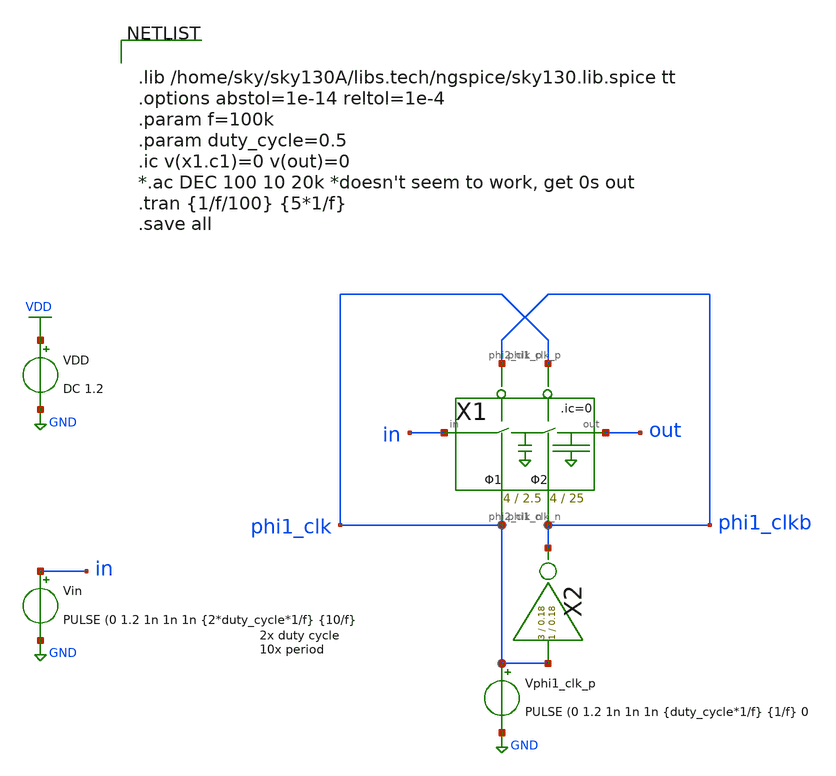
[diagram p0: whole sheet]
** sch_path: xschem/Switched_Caps/2switchcaps_tb.sch
**.subckt 2switchcaps_tb
Vin in GND PULSE (0 1.2 1n 1n 1n {2*duty_cycle*1/f} {10/f}
X1 in out phi1_clkb phi1_clk phi1_clkb phi1_clk 2switchcaps Wcap1=4 Lcap1=2.5 Wcap2=4 Lcap2=25
VDD VDD GND DC 1.2
X2 phi1_clk phi1_clkb inv Wpmos=3 Lpmos=0.18 Wnmos=1 Lnmos=0.18
Vphi1_clk_p phi1_clk GND PULSE (0 1.2 1n 1n 1n {duty_cycle*1/f} {1/f} 0
**** begin user architecture code


.lib /home/sky/sky130A/libs.tech/ngspice/sky130.lib.spice tt
.options abstol=1e-14 reltol=1e-4
.param f=100k
.param duty_cycle=0.5
.ic v(x1.c1)=0 v(out)=0
*.ac DEC 100 10 20k *doesn't seem to work, get 0s out
.tran {1/f/100} {5*1/f}
.save all


**** end user architecture code
**.ends

* expanding   symbol:  Switched_Caps/2switchcaps.sym # of pins=6
** sym_path: xschem/Switched_Caps/2switchcaps.sym
** sch_path: xschem/Switched_Caps/2switchcaps.sch
.subckt 2switchcaps in out phi2_clk_n phi1_clk_n phi1_clk_p phi2_clk_p  Wcap1=4 Lcap1=2.5 Wcap2=4 Lcap2=25
*.iopin out
*.iopin in
*.ipin phi1_clk_n
*.ipin phi1_clk_p
*.ipin phi2_clk_p
*.ipin phi2_clk_n
XC1 c1 GND sky130_fd_pr__cap_mim_m3_1 W=Wcap L=Lcap MF=1 m=1
XC2 out GND sky130_fd_pr__cap_mim_m3_1 W=Wcap L=Lcap MF=1 m=1
**** begin user architecture code

.ic v(c1)=0 v(out)=0

**** end user architecture code
X1 in c1 phi1_clk_p phi1_clk_n transmission_gate Wpmos=3 Lpmos=0.18 Wnmos=1 Lnmos=0.18
X2 c1 out phi2_clk_p phi2_clk_n transmission_gate Wpmos=3 Lpmos=0.18 Wnmos=1 Lnmos=0.18
.ends


* expanding   symbol:  inv/inv.sym # of pins=2
** sym_path: xschem/inv/inv.sym
** sch_path: xschem/inv/inv.sch
.subckt inv in out  Wpmos=3 Lpmos=0.18 Wnmos=1 Lnmos=0.18
*.ipin in
*.iopin out
XM1 out in GND GND sky130_fd_pr__nfet_01v8 L=Lnmos W=Wnmos nf=1 ad='int((nf+1)/2) * W/nf * 0.29' as='int((nf+2)/2)
+ * W/nf * 0.29' pd='2*int((nf+1)/2) * (W/nf + 0.29)' ps='2*int((nf+2)/2) * (W/nf + 0.29)' nrd='0.29 /
+ W' nrs='0.29 / W' sa=0 sb=0 sd=0 mult=1 m=1
XM2 out in VDD VDD sky130_fd_pr__pfet_01v8 L=Lpmos W=Wpmos nf=1 ad='int((nf+1)/2) * W/nf * 0.29' as='int((nf+2)/2)
+ * W/nf * 0.29' pd='2*int((nf+1)/2) * (W/nf + 0.29)' ps='2*int((nf+2)/2) * (W/nf + 0.29)' nrd='0.29 /
+ W' nrs='0.29 / W' sa=0 sb=0 sd=0 mult=1 m=1
.ends


* expanding   symbol:  transmission_gate/transmission_gate.sym # of pins=4
** sym_path: xschem/transmission_gate/transmission_gate.sym
** sch_path: xschem/transmission_gate/transmission_gate.sch
.subckt transmission_gate in out ctrl_ ctrl  Wpmos=1 Lpmos=0.18 Wnmos=1 Lnmos=0.18
*.iopin in
*.iopin out
*.ipin ctrl_
*.ipin ctrl
XM1 in ctrl out GND sky130_fd_pr__nfet_01v8 L=Lnmos W=Wnmos nf=1 ad='int((nf+1)/2) * W/nf * 0.29' as='int((nf+2)/2)
+ * W/nf * 0.29' pd='2*int((nf+1)/2) * (W/nf + 0.29)' ps='2*int((nf+2)/2) * (W/nf + 0.29)' nrd='0.29 /
+ W' nrs='0.29 / W' sa=0 sb=0 sd=0 mult=1 m=1
XM2 out ctrl_ in VDD sky130_fd_pr__pfet_01v8 L=Lpmos W=Wpmos nf=1 ad='int((nf+1)/2) * W/nf * 0.29' as='int((nf+2)/2)
+ * W/nf * 0.29' pd='2*int((nf+1)/2) * (W/nf + 0.29)' ps='2*int((nf+2)/2) * (W/nf + 0.29)' nrd='0.29 /
+ W' nrs='0.29 / W' sa=0 sb=0 sd=0 mult=1 m=1
.ends

.GLOBAL GND
.GLOBAL VDD
.end
